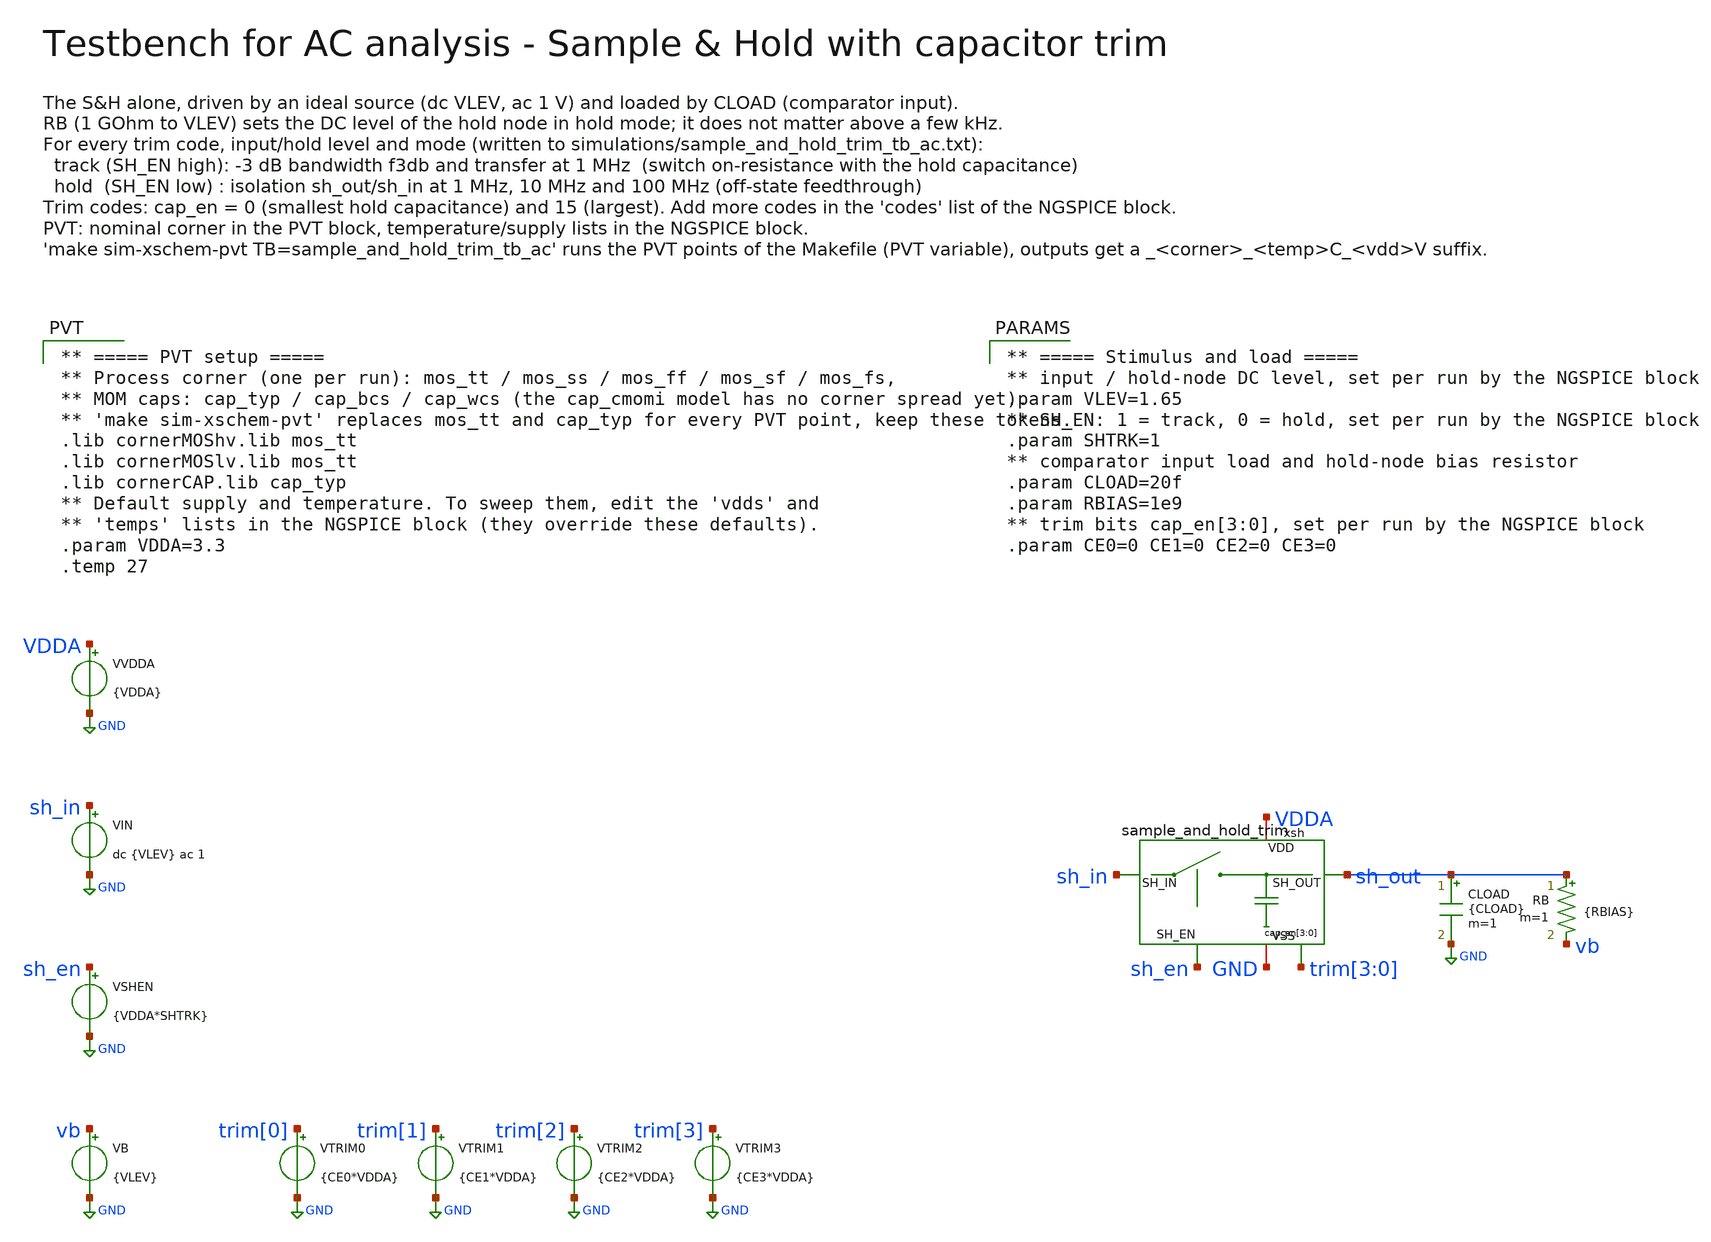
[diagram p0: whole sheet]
** sch_path: macros/heichips26_FAIf/macros/sample_and_hold_trim/testbenches/xschem/sample_and_hold_trim_tb_ac.sch
**.subckt sample_and_hold_trim_tb_ac
VVDDA VDDA GND {VDDA}
VIN sh_in GND dc {VLEV} ac 1
VSHEN sh_en GND {VDDA*SHTRK}
VB vb GND {VLEV}
VTRIM0 trim[0] GND {CE0*VDDA}
VTRIM1 trim[1] GND {CE1*VDDA}
VTRIM2 trim[2] GND {CE2*VDDA}
VTRIM3 trim[3] GND {CE3*VDDA}
xsh VDDA sh_in sh_out sh_en GND trim[3] trim[2] trim[1] trim[0] sample_and_hold_trim
CLOAD sh_out GND {CLOAD} m=1
RB sh_out vb {RBIAS} m=1
**** begin user architecture code
 ** ===== PVT setup =====
** Process corner (one per run): mos_tt / mos_ss / mos_ff / mos_sf / mos_fs,
** MOM caps: cap_typ / cap_bcs / cap_wcs (the cap_cmomi model has no corner spread yet).
** 'make sim-xschem-pvt' replaces mos_tt and cap_typ for every PVT point, keep these tokens.
.lib cornerMOShv.lib mos_tt
.lib cornerMOSlv.lib mos_tt
.lib cornerCAP.lib cap_typ
** Default supply and temperature. To sweep them, edit the 'vdds' and
** 'temps' lists in the NGSPICE block (they override these defaults).
.param VDDA=3.3
.temp 27


** ===== Stimulus and load =====
** input / hold-node DC level, set per run by the NGSPICE block
.param VLEV=1.65
** SH_EN: 1 = track, 0 = hold, set per run by the NGSPICE block
.param SHTRK=1
** comparator input load and hold-node bias resistor
.param CLOAD=20f
.param RBIAS=1e9
** trim bits cap_en[3:0], set per run by the NGSPICE block
.param CE0=0 CE1=0 CE2=0 CE3=0




** same solver settings as the transient testbenches
.options method=gear reltol=1e-4 abstol=1e-15 gmin=1e-18
.control
  ** ===== sweep lists =====
  ** trim codes for cap_en[3:0]: 0 = smallest, 15 = largest hold capacitance
  set codes = ( 0 15 )
  ** DC level of the input (track) / of the hold node (hold)
  set levels = ( 0.5 1.65 2.8 )
  ** temperature and supply sweep lists (process corner: see PVT block)
  set temps = ( 27 )
  set vdds = ( 3.3 )
  ** 'make sim-xschem-pvt' passes the PVT point with ngspice -D and adds a
  ** _<corner>_<temp>C_<vdd>V suffix to the output files
  if $?pvt_temp
    set temps = ( $pvt_temp )
  end
  if $?pvt_vdd
    set vdds = ( $pvt_vdd )
  end
  if $?pvt_corner
  else
    set pvt_corner = tt
  end
  set ext_txt = .txt
  set ext_raw = .raw
  ** output names: <tb><pvt_tag>.<ext>, the tag only exists for PVT runs
  if $?pvt_tag
    set outtxt = "@schname\$pvt_tag$ext_txt"
    set outraw = "@schname\$pvt_tag$ext_raw"
  else
    set outtxt = "@schname\$ext_txt"
    set outraw = "@schname\$ext_raw"
  end

  echo corner temp_C vdd_V code mode vin_V f3db_MHz gain_1MHz_dB iso_1MHz_dB iso_10MHz_dB
+ iso_100MHz_dB > $outtxt
  unset appendwrite
  foreach temp_c $temps
  foreach vdd $vdds
  foreach code $codes
    ** split the trim code into the cap_en bits
    let b0 = $code - 2*floor($code/2)
    let b1 = floor($code/2) - 2*floor($code/4)
    let b2 = floor($code/4) - 2*floor($code/8)
    let b3 = floor($code/8) - 2*floor($code/16)
    foreach lev $levels
    ** shtrk = 1: SH_EN high (track), 0: SH_EN low (hold)
    foreach shtrk 1 0
      alterparam VDDA = $vdd
      alterparam CE0 = $&b0
      alterparam CE1 = $&b1
      alterparam CE2 = $&b2
      alterparam CE3 = $&b3
      alterparam VLEV = $lev
      alterparam SHTRK = $shtrk
      reset
      ** set the temperature after reset (reset restores the netlist temperature)
      option temp = $temp_c
      save v(sh_in) v(sh_out)
      ac dec 20 1k 1G
      write $outraw
      set appendwrite
      ** transfer sh_out/sh_in in dB (sh_in is the ideal 1 V AC source)
      let tf_db = vdb(sh_out)
      meas ac a1m find tf_db at=1e6
      if $shtrk = 1
        meas ac amin min tf_db
        if amin < -3
          meas ac f3db when tf_db=-3 fall=1
          let f3db_mhz = f3db/1e6
          echo $pvt_corner $temp_c $vdd $code track $lev $&f3db_mhz $&a1m - - - >> $outtxt
        else
          ** no -3 dB point below 1 GHz
          echo $pvt_corner $temp_c $vdd $code track $lev over_1000 $&a1m - - - >> $outtxt
        end
      else
        meas ac a10m find tf_db at=1e7
        meas ac a100m find tf_db at=1e8
        echo $pvt_corner $temp_c $vdd $code hold $lev - - $&a1m $&a10m $&a100m >> $outtxt
      end
    end
    end
  end
  end
  end
  echo
  echo ===== Results: simulations/$outtxt =====
  shell cat $outtxt
.endc


**** end user architecture code
**.ends
.GLOBAL GND
.end
